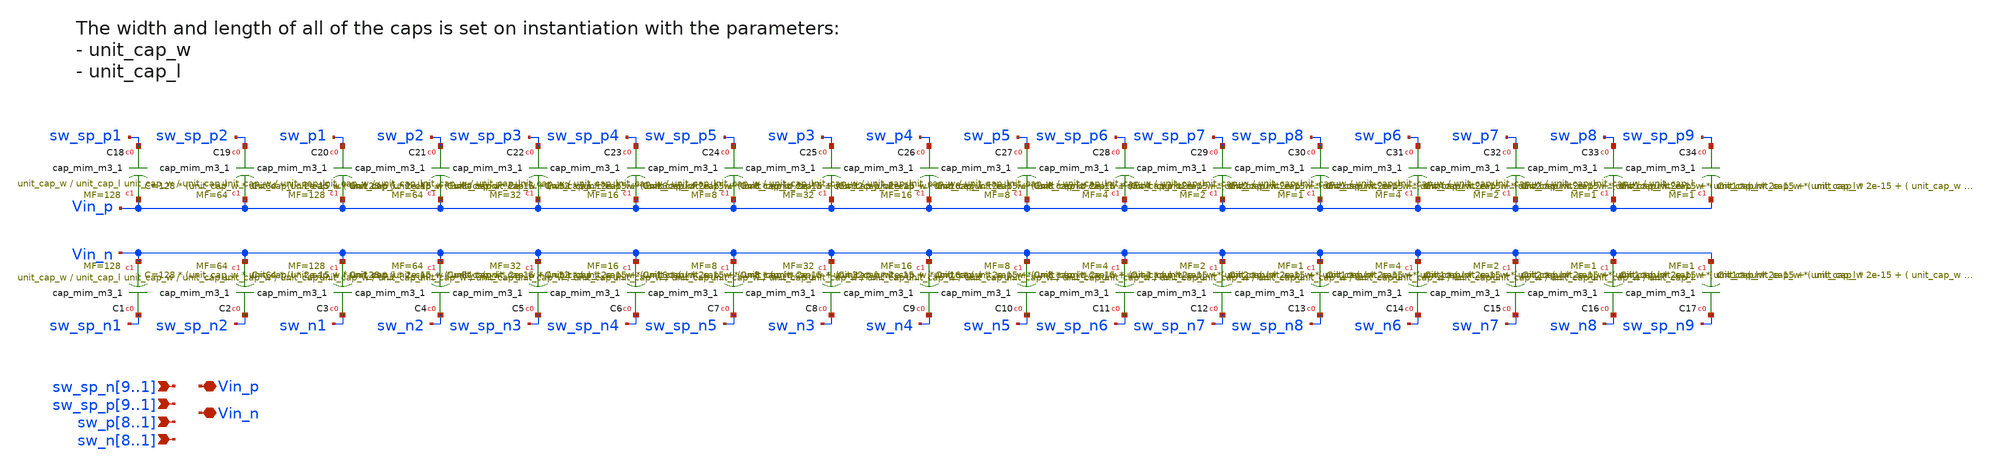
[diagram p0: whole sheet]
** sch_path: xschem/src/capacitor_array/capacitor_array.sch
**.subckt capacitor_array
*+ sw_sp_n9,sw_sp_n8,sw_sp_n7,sw_sp_n6,sw_sp_n5,sw_sp_n4,sw_sp_n3,sw_sp_n2,sw_sp_n1 Vin_p Vin_n sw_sp_p9,sw_sp_p8,sw_sp_p7,sw_sp_p6,sw_sp_p5,sw_sp_p4,sw_sp_p3,sw_sp_p2,sw_sp_p1
*+ sw_p8,sw_p7,sw_p6,sw_p5,sw_p4,sw_p3,sw_p2,sw_p1 sw_n8,sw_n7,sw_n6,sw_n5,sw_n4,sw_n3,sw_n2,sw_n1
*.ipin sw_sp_n9,sw_sp_n8,sw_sp_n7,sw_sp_n6,sw_sp_n5,sw_sp_n4,sw_sp_n3,sw_sp_n2,sw_sp_n1
*.iopin Vin_p
*.iopin Vin_n
*.ipin sw_sp_p9,sw_sp_p8,sw_sp_p7,sw_sp_p6,sw_sp_p5,sw_sp_p4,sw_sp_p3,sw_sp_p2,sw_sp_p1
*.ipin sw_p8,sw_p7,sw_p6,sw_p5,sw_p4,sw_p3,sw_p2,sw_p1
*.ipin sw_n8,sw_n7,sw_n6,sw_n5,sw_n4,sw_n3,sw_n2,sw_n1
XC1 sw_sp_n1 Vin_n sky130_fd_pr__cap_mim_m3_1 W=unit_cap_w L=unit_cap_l MF=128 m=128
XC2 sw_sp_n2 Vin_n sky130_fd_pr__cap_mim_m3_1 W=unit_cap_w L=unit_cap_l MF=64 m=64
XC3 sw_n1 Vin_n sky130_fd_pr__cap_mim_m3_1 W=unit_cap_w L=unit_cap_l MF=128 m=128
XC4 sw_n2 Vin_n sky130_fd_pr__cap_mim_m3_1 W=unit_cap_w L=unit_cap_l MF=64 m=64
XC5 sw_sp_n3 Vin_n sky130_fd_pr__cap_mim_m3_1 W=unit_cap_w L=unit_cap_l MF=32 m=32
XC6 sw_sp_n4 Vin_n sky130_fd_pr__cap_mim_m3_1 W=unit_cap_w L=unit_cap_l MF=16 m=16
XC7 sw_sp_n5 Vin_n sky130_fd_pr__cap_mim_m3_1 W=unit_cap_w L=unit_cap_l MF=8 m=8
XC8 sw_n3 Vin_n sky130_fd_pr__cap_mim_m3_1 W=unit_cap_w L=unit_cap_l MF=32 m=32
XC9 sw_n4 Vin_n sky130_fd_pr__cap_mim_m3_1 W=unit_cap_w L=unit_cap_l MF=16 m=16
XC10 sw_n5 Vin_n sky130_fd_pr__cap_mim_m3_1 W=unit_cap_w L=unit_cap_l MF=8 m=8
XC11 sw_sp_n6 Vin_n sky130_fd_pr__cap_mim_m3_1 W=unit_cap_w L=unit_cap_l MF=4 m=4
XC12 sw_sp_n7 Vin_n sky130_fd_pr__cap_mim_m3_1 W=unit_cap_w L=unit_cap_l MF=2 m=2
XC13 sw_sp_n8 Vin_n sky130_fd_pr__cap_mim_m3_1 W=unit_cap_w L=unit_cap_l MF=1 m=1
XC14 sw_n6 Vin_n sky130_fd_pr__cap_mim_m3_1 W=unit_cap_w L=unit_cap_l MF=4 m=4
XC15 sw_n7 Vin_n sky130_fd_pr__cap_mim_m3_1 W=unit_cap_w L=unit_cap_l MF=2 m=2
XC16 sw_n8 Vin_n sky130_fd_pr__cap_mim_m3_1 W=unit_cap_w L=unit_cap_l MF=1 m=1
XC17 sw_sp_n9 Vin_n sky130_fd_pr__cap_mim_m3_1 W=unit_cap_w L=unit_cap_l MF=1 m=1
XC18 sw_sp_p1 Vin_p sky130_fd_pr__cap_mim_m3_1 W=unit_cap_w L=unit_cap_l MF=128 m=128
XC19 sw_sp_p2 Vin_p sky130_fd_pr__cap_mim_m3_1 W=unit_cap_w L=unit_cap_l MF=64 m=64
XC20 sw_p1 Vin_p sky130_fd_pr__cap_mim_m3_1 W=unit_cap_w L=unit_cap_l MF=128 m=128
XC21 sw_p2 Vin_p sky130_fd_pr__cap_mim_m3_1 W=unit_cap_w L=unit_cap_l MF=64 m=64
XC22 sw_sp_p3 Vin_p sky130_fd_pr__cap_mim_m3_1 W=unit_cap_w L=unit_cap_l MF=32 m=32
XC23 sw_sp_p4 Vin_p sky130_fd_pr__cap_mim_m3_1 W=unit_cap_w L=unit_cap_l MF=16 m=16
XC24 sw_sp_p5 Vin_p sky130_fd_pr__cap_mim_m3_1 W=unit_cap_w L=unit_cap_l MF=8 m=8
XC25 sw_p3 Vin_p sky130_fd_pr__cap_mim_m3_1 W=unit_cap_w L=unit_cap_l MF=32 m=32
XC26 sw_p4 Vin_p sky130_fd_pr__cap_mim_m3_1 W=unit_cap_w L=unit_cap_l MF=16 m=16
XC27 sw_p5 Vin_p sky130_fd_pr__cap_mim_m3_1 W=unit_cap_w L=unit_cap_l MF=8 m=8
XC28 sw_sp_p6 Vin_p sky130_fd_pr__cap_mim_m3_1 W=unit_cap_w L=unit_cap_l MF=4 m=4
XC29 sw_sp_p7 Vin_p sky130_fd_pr__cap_mim_m3_1 W=unit_cap_w L=unit_cap_l MF=2 m=2
XC30 sw_sp_p8 Vin_p sky130_fd_pr__cap_mim_m3_1 W=unit_cap_w L=unit_cap_l MF=1 m=1
XC31 sw_p6 Vin_p sky130_fd_pr__cap_mim_m3_1 W=unit_cap_w L=unit_cap_l MF=4 m=4
XC32 sw_p7 Vin_p sky130_fd_pr__cap_mim_m3_1 W=unit_cap_w L=unit_cap_l MF=2 m=2
XC33 sw_p8 Vin_p sky130_fd_pr__cap_mim_m3_1 W=unit_cap_w L=unit_cap_l MF=1 m=1
XC34 sw_sp_p9 Vin_p sky130_fd_pr__cap_mim_m3_1 W=unit_cap_w L=unit_cap_l MF=1 m=1
**.ends
.end
